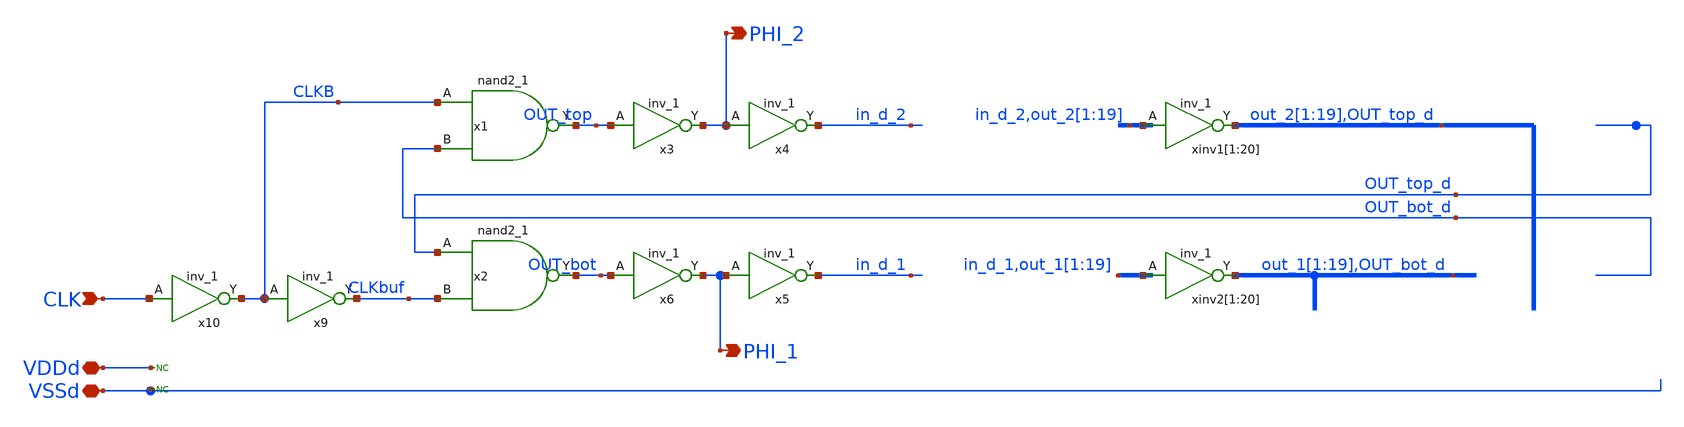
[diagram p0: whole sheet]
** sch_path: NO_ClkGen/NO_ClkGen._w_cap.sch
**.subckt NO_ClkGen._w_cap CLK PHI_2 PHI_1 VDDd VSSd
*.ipin CLK
*.opin PHI_2
*.opin PHI_1
*.iopin VDDd
*.iopin VSSd
x1 CLKB OUT_bot_d VSSd VDDd VSSd VDDd OUT_top gf180mcu_fd_sc_mcu9t5v0__nand2_1
x2 OUT_top_d CLKbuf VSSd VDDd VSSd VDDd OUT_bot gf180mcu_fd_sc_mcu9t5v0__nand2_1
x3 OUT_top VSSd VDDd VSSd VDDd PHI_2 gf180mcu_fd_sc_mcu9t5v0__inv_1
x4 PHI_2 VSSd VDDd VSSd VDDd in_d_2 gf180mcu_fd_sc_mcu9t5v0__inv_1
x6 OUT_bot VSSd VDDd VSSd VDDd PHI_1 gf180mcu_fd_sc_mcu9t5v0__inv_1
x9 CLKB VSSd VDDd VSSd VDDd CLKbuf gf180mcu_fd_sc_mcu9t5v0__inv_1
x10 CLK VSSd VDDd VSSd VDDd CLKB gf180mcu_fd_sc_mcu9t5v0__inv_1
* noconn VDDd
* noconn VSSd
xinv1[1] in_d_2 VSSd VDDd VSSd VDDd out_2[1] gf180mcu_fd_sc_mcu9t5v0__inv_1
xinv1[2] out_2[1] VSSd VDDd VSSd VDDd out_2[2] gf180mcu_fd_sc_mcu9t5v0__inv_1
xinv1[3] out_2[2] VSSd VDDd VSSd VDDd out_2[3] gf180mcu_fd_sc_mcu9t5v0__inv_1
xinv1[4] out_2[3] VSSd VDDd VSSd VDDd out_2[4] gf180mcu_fd_sc_mcu9t5v0__inv_1
xinv1[5] out_2[4] VSSd VDDd VSSd VDDd out_2[5] gf180mcu_fd_sc_mcu9t5v0__inv_1
xinv1[6] out_2[5] VSSd VDDd VSSd VDDd out_2[6] gf180mcu_fd_sc_mcu9t5v0__inv_1
xinv1[7] out_2[6] VSSd VDDd VSSd VDDd out_2[7] gf180mcu_fd_sc_mcu9t5v0__inv_1
xinv1[8] out_2[7] VSSd VDDd VSSd VDDd out_2[8] gf180mcu_fd_sc_mcu9t5v0__inv_1
xinv1[9] out_2[8] VSSd VDDd VSSd VDDd out_2[9] gf180mcu_fd_sc_mcu9t5v0__inv_1
xinv1[10] out_2[9] VSSd VDDd VSSd VDDd out_2[10] gf180mcu_fd_sc_mcu9t5v0__inv_1
xinv1[11] out_2[10] VSSd VDDd VSSd VDDd out_2[11] gf180mcu_fd_sc_mcu9t5v0__inv_1
xinv1[12] out_2[11] VSSd VDDd VSSd VDDd out_2[12] gf180mcu_fd_sc_mcu9t5v0__inv_1
xinv1[13] out_2[12] VSSd VDDd VSSd VDDd out_2[13] gf180mcu_fd_sc_mcu9t5v0__inv_1
xinv1[14] out_2[13] VSSd VDDd VSSd VDDd out_2[14] gf180mcu_fd_sc_mcu9t5v0__inv_1
xinv1[15] out_2[14] VSSd VDDd VSSd VDDd out_2[15] gf180mcu_fd_sc_mcu9t5v0__inv_1
xinv1[16] out_2[15] VSSd VDDd VSSd VDDd out_2[16] gf180mcu_fd_sc_mcu9t5v0__inv_1
xinv1[17] out_2[16] VSSd VDDd VSSd VDDd out_2[17] gf180mcu_fd_sc_mcu9t5v0__inv_1
xinv1[18] out_2[17] VSSd VDDd VSSd VDDd out_2[18] gf180mcu_fd_sc_mcu9t5v0__inv_1
xinv1[19] out_2[18] VSSd VDDd VSSd VDDd out_2[19] gf180mcu_fd_sc_mcu9t5v0__inv_1
xinv1[20] out_2[19] VSSd VDDd VSSd VDDd OUT_top_d gf180mcu_fd_sc_mcu9t5v0__inv_1
x5 PHI_1 VSSd VDDd VSSd VDDd in_d_1 gf180mcu_fd_sc_mcu9t5v0__inv_1
xinv2[1] in_d_1 VSSd VDDd VSSd VDDd out_1[1] gf180mcu_fd_sc_mcu9t5v0__inv_1
xinv2[2] out_1[1] VSSd VDDd VSSd VDDd out_1[2] gf180mcu_fd_sc_mcu9t5v0__inv_1
xinv2[3] out_1[2] VSSd VDDd VSSd VDDd out_1[3] gf180mcu_fd_sc_mcu9t5v0__inv_1
xinv2[4] out_1[3] VSSd VDDd VSSd VDDd out_1[4] gf180mcu_fd_sc_mcu9t5v0__inv_1
xinv2[5] out_1[4] VSSd VDDd VSSd VDDd out_1[5] gf180mcu_fd_sc_mcu9t5v0__inv_1
xinv2[6] out_1[5] VSSd VDDd VSSd VDDd out_1[6] gf180mcu_fd_sc_mcu9t5v0__inv_1
xinv2[7] out_1[6] VSSd VDDd VSSd VDDd out_1[7] gf180mcu_fd_sc_mcu9t5v0__inv_1
xinv2[8] out_1[7] VSSd VDDd VSSd VDDd out_1[8] gf180mcu_fd_sc_mcu9t5v0__inv_1
xinv2[9] out_1[8] VSSd VDDd VSSd VDDd out_1[9] gf180mcu_fd_sc_mcu9t5v0__inv_1
xinv2[10] out_1[9] VSSd VDDd VSSd VDDd out_1[10] gf180mcu_fd_sc_mcu9t5v0__inv_1
xinv2[11] out_1[10] VSSd VDDd VSSd VDDd out_1[11] gf180mcu_fd_sc_mcu9t5v0__inv_1
xinv2[12] out_1[11] VSSd VDDd VSSd VDDd out_1[12] gf180mcu_fd_sc_mcu9t5v0__inv_1
xinv2[13] out_1[12] VSSd VDDd VSSd VDDd out_1[13] gf180mcu_fd_sc_mcu9t5v0__inv_1
xinv2[14] out_1[13] VSSd VDDd VSSd VDDd out_1[14] gf180mcu_fd_sc_mcu9t5v0__inv_1
xinv2[15] out_1[14] VSSd VDDd VSSd VDDd out_1[15] gf180mcu_fd_sc_mcu9t5v0__inv_1
xinv2[16] out_1[15] VSSd VDDd VSSd VDDd out_1[16] gf180mcu_fd_sc_mcu9t5v0__inv_1
xinv2[17] out_1[16] VSSd VDDd VSSd VDDd out_1[17] gf180mcu_fd_sc_mcu9t5v0__inv_1
xinv2[18] out_1[17] VSSd VDDd VSSd VDDd out_1[18] gf180mcu_fd_sc_mcu9t5v0__inv_1
xinv2[19] out_1[18] VSSd VDDd VSSd VDDd out_1[19] gf180mcu_fd_sc_mcu9t5v0__inv_1
xinv2[20] out_1[19] VSSd VDDd VSSd VDDd OUT_bot_d gf180mcu_fd_sc_mcu9t5v0__inv_1
**.ends
.end
